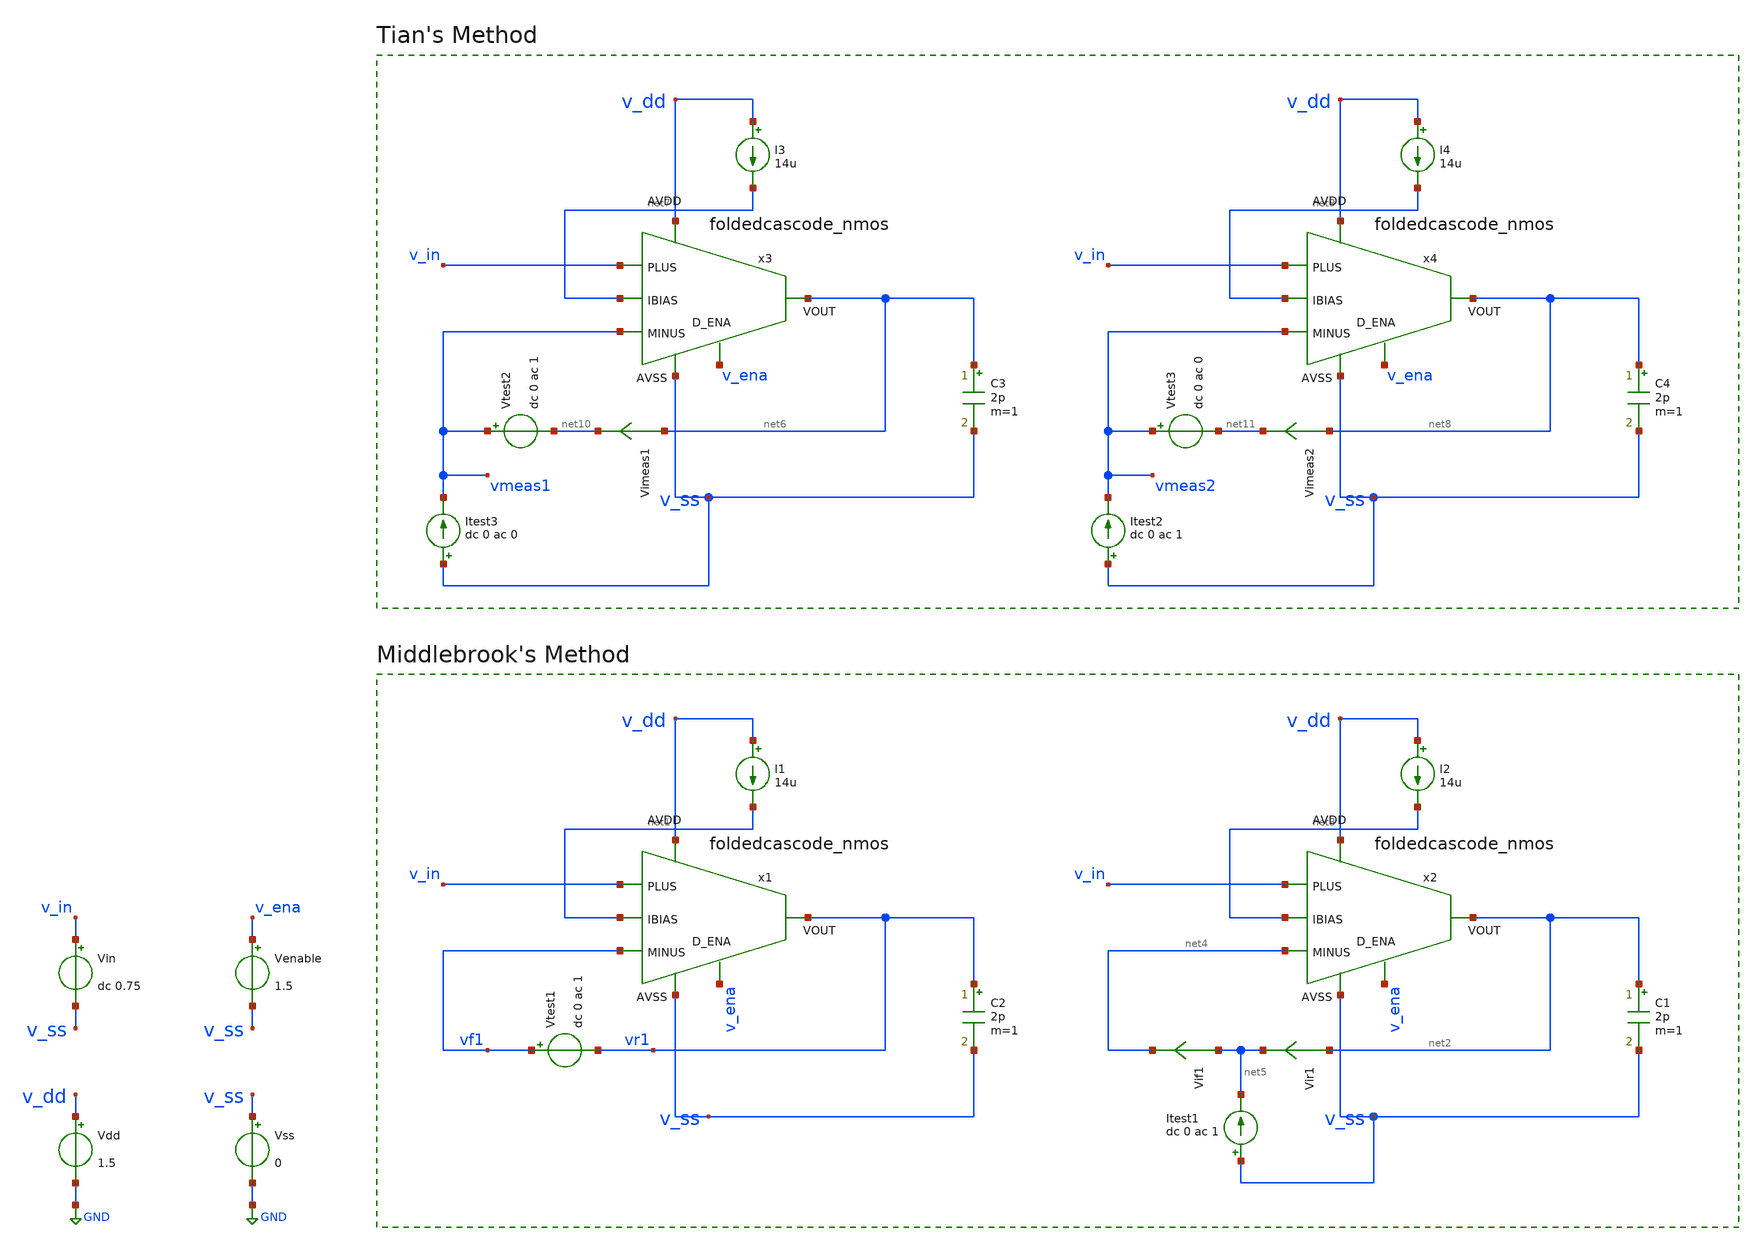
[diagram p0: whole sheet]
** sch_path: Designs/otas/1_schematics/tb_foldedcascode_nmos_loopgain.sch
* (c) 2025 Thesis_HP, Apache-2.0 license
**.subckt tb_foldedcascode_nmos_loopgain
Vdd v_dd GND 1.5
Vss v_ss GND 0
Vin v_in v_ss dc 0.75
C2 vr1 v_ss 2p m=1
I1 v_dd net1 14u
Vtest1 vf1 vr1 dc 0 ac 1
C1 net2 v_ss 2p m=1
I2 v_dd net3 14u
Vir1 net2 net5 0
.save i(vir1)
Vif1 net5 net4 0
.save i(vif1)
Itest1 v_ss net5 dc 0 ac 1
C3 net6 v_ss 2p m=1
I3 v_dd net7 14u
C4 net8 v_ss 2p m=1
I4 v_dd net9 14u
Itest3 v_ss vmeas1 dc 0 ac 0
Vtest2 vmeas1 net10 dc 0 ac 1
Vimeas1 net6 net10 0
.save i(vimeas1)
Itest2 v_ss vmeas2 dc 0 ac 1
Vtest3 vmeas2 net11 dc 0 ac 0
Vimeas2 net8 net11 0
.save i(vimeas2)
x3 v_dd net7 net6 vmeas1 v_in v_ena v_ss foldedcascode_nmos
x4 v_dd net9 net8 vmeas2 v_in v_ena v_ss foldedcascode_nmos
x1 v_dd net1 vr1 vf1 v_in v_ena v_ss foldedcascode_nmos
x2 v_dd net3 net2 net4 v_in v_ena v_ss foldedcascode_nmos
Venable v_ena v_ss 1.5
**** begin user architecture code

.lib cornerMOSlv.lib mos_tt
.lib cornerRES.lib res_typ




*.include /foss/designs/thesis/thesis_hp/designs/otas/3_kpex/foldedcascode_nmos_withdummies__foldedcascode_nmos_withdummies/magic_CC/foldedcascode_nmos_withdummies.pex.spice


.param temp=27
.options savecurrents reltol=1e-3 abstol=1e-12 gmin=1e-15
.control
save all

* Operating Point Analysis
op
remzerovec
write foldedcascode_nmos_tb-loopgain.raw
set appendwrite

* AC Analysis
ac dec 101 1 100G
remzerovec
write foldedcascode_nmos_tb-loopgain.raw
set appendwrite

* Middlebrook's Method
let tv=-v(vr1)/v(vf1)
let ti=-i(vir1)/i(vif1)
let tmb=(tv*ti - 1)/(tv + ti + 2)

plot db(tmb) ylabel 'Magnitude - Middlebrook'
plot 180/pi*cphase(tmb) ylabel 'Phase - Middlebrook'

* Tian's Method
* vtest=0, itest=1:
let A=i(Vimeas2)
let C=v(vmeas2)

* vtest=1, itest=0:
let B=i(Vimeas1)
let D=v(vmeas1)
let ttian=(A*D-B*C-A)/(2*(B*C-A*D)+A-D+1)

plot db(ttian) ylabel 'Magnitude - Tian'
plot 180/pi*cphase(ttian) ylabel 'Phase - Tian'

* Middlebrook vs. Tian
plot db(tmb) db(ttian) ylabel 'Magnitude'
plot 180/pi*cphase(tmb) 180/pi*cphase(ttian) ylabel 'Phase'

write foldedcascode_nmos_tb-loopgain.raw

*quit
.endc


**** end user architecture code
**.ends
.GLOBAL GND
.end
